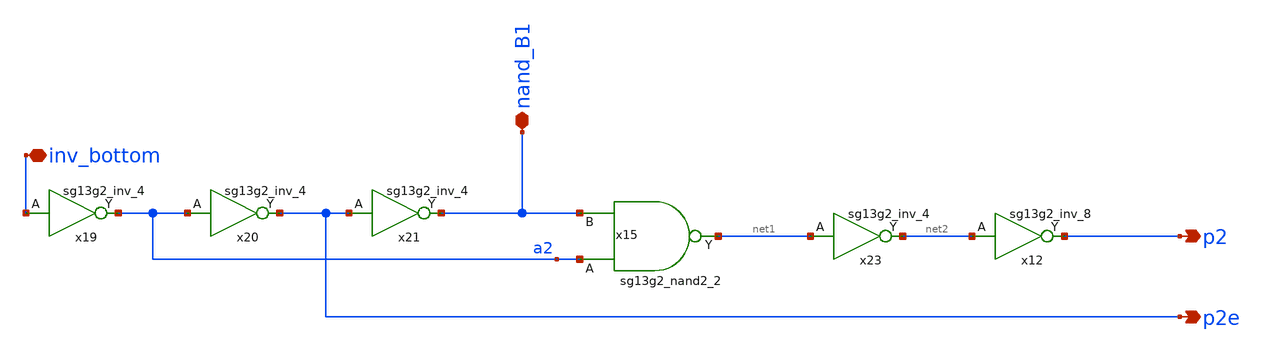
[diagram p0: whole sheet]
** sch_path: 5_Design/4_Layout/Team 5/splitUpSimulationsAndSchematics/clock_5_split2.sch
* IHP-GmbH/IHP-Open-PDK/ihp-sg13g2/libs.tech/xschem/sg13g2_stdcells/sg13g2_inv_4.sch:
* Copyright 2023 IHP PDK Authors
* Licensed under the Apache License, Version 2.0 (the "License");
**.subckt clock_5_split2 p2 p2e inv_bottom nand_B1
*.opin p2
*.opin p2e
*.iopin inv_bottom
*.iopin nand_B1
x19 a2 inv_bottom VDD VSS sg13g2_inv_4
x20 p2e a2 VDD VSS sg13g2_inv_4
x21 nand_B1 p2e VDD VSS sg13g2_inv_4
x23 net2 net1 VDD VSS sg13g2_inv_4
x12 p2 net2 VDD VSS sg13g2_inv_8
x15 net1 a2 nand_B1 VDD VSS sg13g2_nand2_2
**.ends

* expanding   symbol:  sg13g2_stdcells/sg13g2_inv_4.sym # of pins=2
** sym_path: sg13g2_stdcells/sg13g2_inv_4.sym
** sch_path: sg13g2_stdcells/sg13g2_inv_4.sch
.subckt sg13g2_inv_4 Y A VDD VSS
*.ipin A
*.opin Y
*.iopin VDD
*.iopin VSS
XM1 Y A VSS VSS sg13_lv_nmos w=2.96u l=130.00n ng=4 m=1 mm_ok=1
XM2 Y A VDD VDD sg13_lv_pmos w=4.48u l=130.00n ng=4 m=1 mm_ok=1
.ends


* expanding   symbol:  sg13g2_stdcells/sg13g2_inv_8.sym # of pins=2
** sym_path: sg13g2_stdcells/sg13g2_inv_8.sym
** sch_path: sg13g2_stdcells/sg13g2_inv_8.sch
.subckt sg13g2_inv_8 Y A VDD VSS
*.opin Y
*.ipin A
*.iopin VDD
*.iopin VSS
XM1 Y A VSS VSS sg13_lv_nmos w=5.92u l=130.00n ng=8 m=1 mm_ok=1
XM2 Y A VDD VDD sg13_lv_pmos w=8.96u l=130.00n ng=8 m=1 mm_ok=1
.ends


* expanding   symbol:  sg13g2_stdcells/sg13g2_nand2_2.sym # of pins=3
** sym_path: sg13g2_stdcells/sg13g2_nand2_2.sym
** sch_path: sg13g2_stdcells/sg13g2_nand2_2.sch
.subckt sg13g2_nand2_2 Y A B VDD VSS
*.iopin VDD
*.iopin VSS
*.opin Y
*.ipin B
*.ipin A
XM1 Y A net1 VSS sg13_lv_nmos w=1.44u l=130.00n ng=2 m=1 mm_ok=1
XM2 net1 B VSS VSS sg13_lv_nmos w=1.44u l=130.00n ng=2 m=1 mm_ok=1
XM3 Y A VDD VDD sg13_lv_pmos w=2.24u l=130.00n ng=2 m=1 mm_ok=1
XM4 Y B VDD VDD sg13_lv_pmos w=2.24u l=130.00n ng=2 m=1 mm_ok=1
.ends

.end
